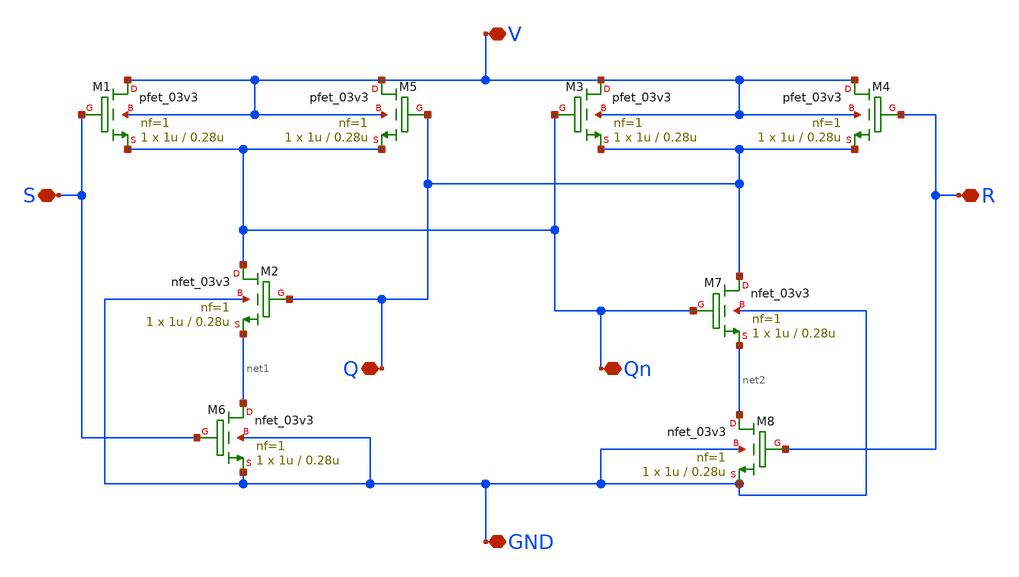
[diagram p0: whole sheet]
** sch_path: SAR_ADC/xschem/designs/SR_nand.sch
**.subckt SR_nand S R V GND Qn Q
*.iopin S
*.iopin R
*.iopin V
*.iopin GND
*.iopin Qn
*.iopin Q
XM1 V S Qn V sky130_fd_pr__pfet_03v3 L=0.28u W=1u nf=1 ad='int((nf+1)/2) * W/nf * 0.18u' as='int((nf+2)/2) * W/nf * 0.18u'
+ pd='2*int((nf+1)/2) * (W/nf + 0.18u)' ps='2*int((nf+2)/2) * (W/nf + 0.18u)' nrd='0.18u / W' nrs='0.18u / W'
+ sa=0 sb=0 sd=0 mult=1 m=1
XM2 Qn Q net1 GND sky130_fd_pr__nfet_03v3 L=0.28u W=1u nf=1 ad='int((nf+1)/2) * W/nf * 0.18u' as='int((nf+2)/2) * W/nf * 0.18u'
+ pd='2*int((nf+1)/2) * (W/nf + 0.18u)' ps='2*int((nf+2)/2) * (W/nf + 0.18u)' nrd='0.18u / W' nrs='0.18u / W'
+ sa=0 sb=0 sd=0 mult=1 m=1
XM3 V Qn Q V sky130_fd_pr__pfet_03v3 L=0.28u W=1u nf=1 ad='int((nf+1)/2) * W/nf * 0.18u' as='int((nf+2)/2) * W/nf * 0.18u'
+ pd='2*int((nf+1)/2) * (W/nf + 0.18u)' ps='2*int((nf+2)/2) * (W/nf + 0.18u)' nrd='0.18u / W' nrs='0.18u / W'
+ sa=0 sb=0 sd=0 mult=1 m=1
XM4 V R Q V sky130_fd_pr__pfet_03v3 L=0.28u W=1u nf=1 ad='int((nf+1)/2) * W/nf * 0.18u' as='int((nf+2)/2) * W/nf * 0.18u'
+ pd='2*int((nf+1)/2) * (W/nf + 0.18u)' ps='2*int((nf+2)/2) * (W/nf + 0.18u)' nrd='0.18u / W' nrs='0.18u / W'
+ sa=0 sb=0 sd=0 mult=1 m=1
XM5 V Q Qn V sky130_fd_pr__pfet_03v3 L=0.28u W=1u nf=1 ad='int((nf+1)/2) * W/nf * 0.18u' as='int((nf+2)/2) * W/nf * 0.18u'
+ pd='2*int((nf+1)/2) * (W/nf + 0.18u)' ps='2*int((nf+2)/2) * (W/nf + 0.18u)' nrd='0.18u / W' nrs='0.18u / W'
+ sa=0 sb=0 sd=0 mult=1 m=1
XM6 net1 S GND GND sky130_fd_pr__nfet_03v3 L=0.28u W=1u nf=1 ad='int((nf+1)/2) * W/nf * 0.18u' as='int((nf+2)/2) * W/nf * 0.18u'
+ pd='2*int((nf+1)/2) * (W/nf + 0.18u)' ps='2*int((nf+2)/2) * (W/nf + 0.18u)' nrd='0.18u / W' nrs='0.18u / W'
+ sa=0 sb=0 sd=0 mult=1 m=1
XM7 Q Qn net2 GND sky130_fd_pr__nfet_03v3 L=0.28u W=1u nf=1 ad='int((nf+1)/2) * W/nf * 0.18u' as='int((nf+2)/2) * W/nf * 0.18u'
+ pd='2*int((nf+1)/2) * (W/nf + 0.18u)' ps='2*int((nf+2)/2) * (W/nf + 0.18u)' nrd='0.18u / W' nrs='0.18u / W'
+ sa=0 sb=0 sd=0 mult=1 m=1
XM8 net2 R GND GND sky130_fd_pr__nfet_03v3 L=0.28u W=1u nf=1 ad='int((nf+1)/2) * W/nf * 0.18u' as='int((nf+2)/2) * W/nf * 0.18u'
+ pd='2*int((nf+1)/2) * (W/nf + 0.18u)' ps='2*int((nf+2)/2) * (W/nf + 0.18u)' nrd='0.18u / W' nrs='0.18u / W'
+ sa=0 sb=0 sd=0 mult=1 m=1
**** begin user architecture code

.include /foss/pdks/gf180mcuC/libs.tech/ngspice/design.ngspice
.lib /foss/pdks/gf180mcuC/libs.tech/ngspice/sm141064.ngspice typical

**** end user architecture code
**.ends
.end
